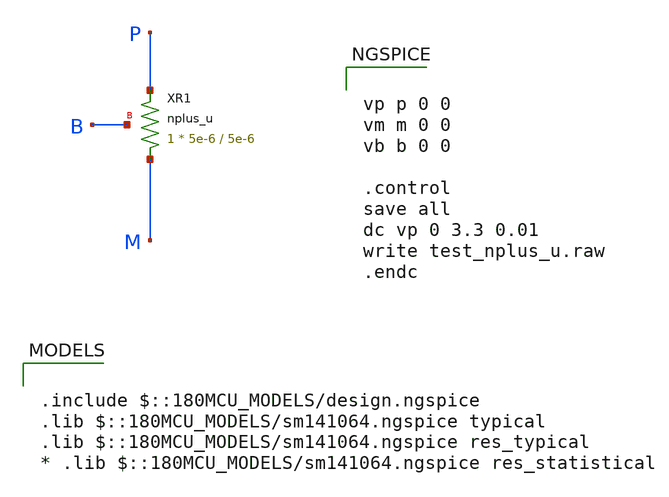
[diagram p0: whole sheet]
** sch_path: gf180mcuD/xschem_libs/gf180mcu_tests/test_nplus_u/schematic/test_nplus_u.sch
* Copyright 2022 GlobalFoundries PDK Authors
* Licensed under the Apache License, Version 2.0 (the "License");
* you may not use this file except in compliance with the License.
* You may obtain a copy of the License at
* https://www.apache.org/licenses/LICENSE-2.0
* Unless required by applicable law or agreed to in writing, software
* distributed under the License is distributed on an "AS IS" BASIS,
* WITHOUT WARRANTIES OR CONDITIONS OF ANY KIND, either express or implied.
* See the License for the specific language governing permissions and
* limitations under the License.
**.subckt test_nplus_u
XR1 M P B nplus_u r_width=5e-6 r_length=5e-6 m=1
**** begin user architecture code

.include $::180MCU_MODELS/design.ngspice
.lib $::180MCU_MODELS/sm141064.ngspice typical
.lib $::180MCU_MODELS/sm141064.ngspice res_typical
* .lib $::180MCU_MODELS/sm141064.ngspice res_statistical



vp p 0 0
vm m 0 0
vb b 0 0

.control
save all
dc vp 0 3.3 0.01
write test_nplus_u.raw
.endc


**** end user architecture code
**.ends
.end
